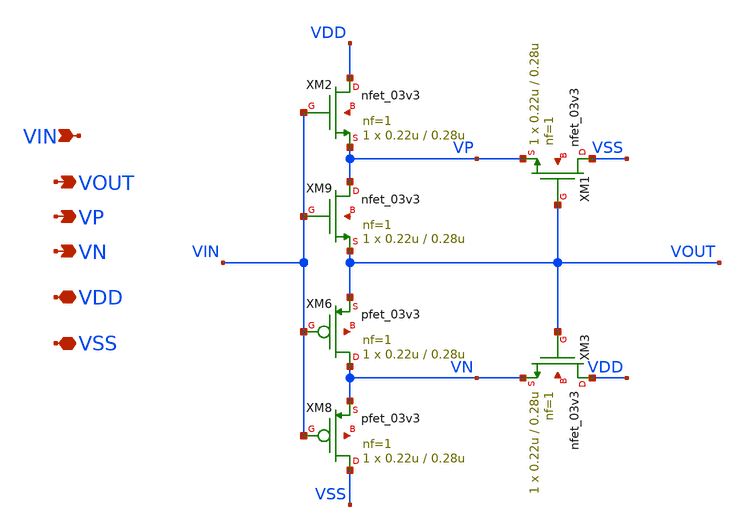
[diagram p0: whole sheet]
** sch_path: analog/schmitt_trigger_comparator/comparator.sch
**.subckt comparator VIN VOUT VDD VSS VN VP
*.ipin VIN
*.opin VOUT
*.iopin VDD
*.iopin VSS
*.opin VN
*.opin VP
XM2 VDD VIN VP net1 nfet_03v3 L=0.28u W=0.22u nf=1 ad='int((nf+1)/2) * W/nf * 0.18u' as='int((nf+2)/2) * W/nf * 0.18u'
+ pd='2*int((nf+1)/2) * (W/nf + 0.18u)' ps='2*int((nf+2)/2) * (W/nf + 0.18u)' nrd='0.18u / W' nrs='0.18u / W'
+ sa=0 sb=0 sd=0 m=1
XM3 VDD VOUT VN net2 nfet_03v3 L=0.28u W=0.22u nf=1 ad='int((nf+1)/2) * W/nf * 0.18u' as='int((nf+2)/2) * W/nf * 0.18u'
+ pd='2*int((nf+1)/2) * (W/nf + 0.18u)' ps='2*int((nf+2)/2) * (W/nf + 0.18u)' nrd='0.18u / W' nrs='0.18u / W'
+ sa=0 sb=0 sd=0 m=1
XM6 VN VIN VOUT net3 pfet_03v3 L=0.28u W=0.22u nf=1 ad='int((nf+1)/2) * W/nf * 0.18u' as='int((nf+2)/2) * W/nf * 0.18u'
+ pd='2*int((nf+1)/2) * (W/nf + 0.18u)' ps='2*int((nf+2)/2) * (W/nf + 0.18u)' nrd='0.18u / W' nrs='0.18u / W'
+ sa=0 sb=0 sd=0 m=1
XM8 VSS VIN VN net4 pfet_03v3 L=0.28u W=0.22u nf=1 ad='int((nf+1)/2) * W/nf * 0.18u' as='int((nf+2)/2) * W/nf * 0.18u'
+ pd='2*int((nf+1)/2) * (W/nf + 0.18u)' ps='2*int((nf+2)/2) * (W/nf + 0.18u)' nrd='0.18u / W' nrs='0.18u / W'
+ sa=0 sb=0 sd=0 m=1
XM9 VP VIN VOUT net5 nfet_03v3 L=0.28u W=0.22u nf=1 ad='int((nf+1)/2) * W/nf * 0.18u' as='int((nf+2)/2) * W/nf * 0.18u'
+ pd='2*int((nf+1)/2) * (W/nf + 0.18u)' ps='2*int((nf+2)/2) * (W/nf + 0.18u)' nrd='0.18u / W' nrs='0.18u / W'
+ sa=0 sb=0 sd=0 m=1
XM1 VSS VOUT VP net6 nfet_03v3 L=0.28u W=0.22u nf=1 ad='int((nf+1)/2) * W/nf * 0.18u' as='int((nf+2)/2) * W/nf * 0.18u'
+ pd='2*int((nf+1)/2) * (W/nf + 0.18u)' ps='2*int((nf+2)/2) * (W/nf + 0.18u)' nrd='0.18u / W' nrs='0.18u / W'
+ sa=0 sb=0 sd=0 m=1
**.ends
.end
